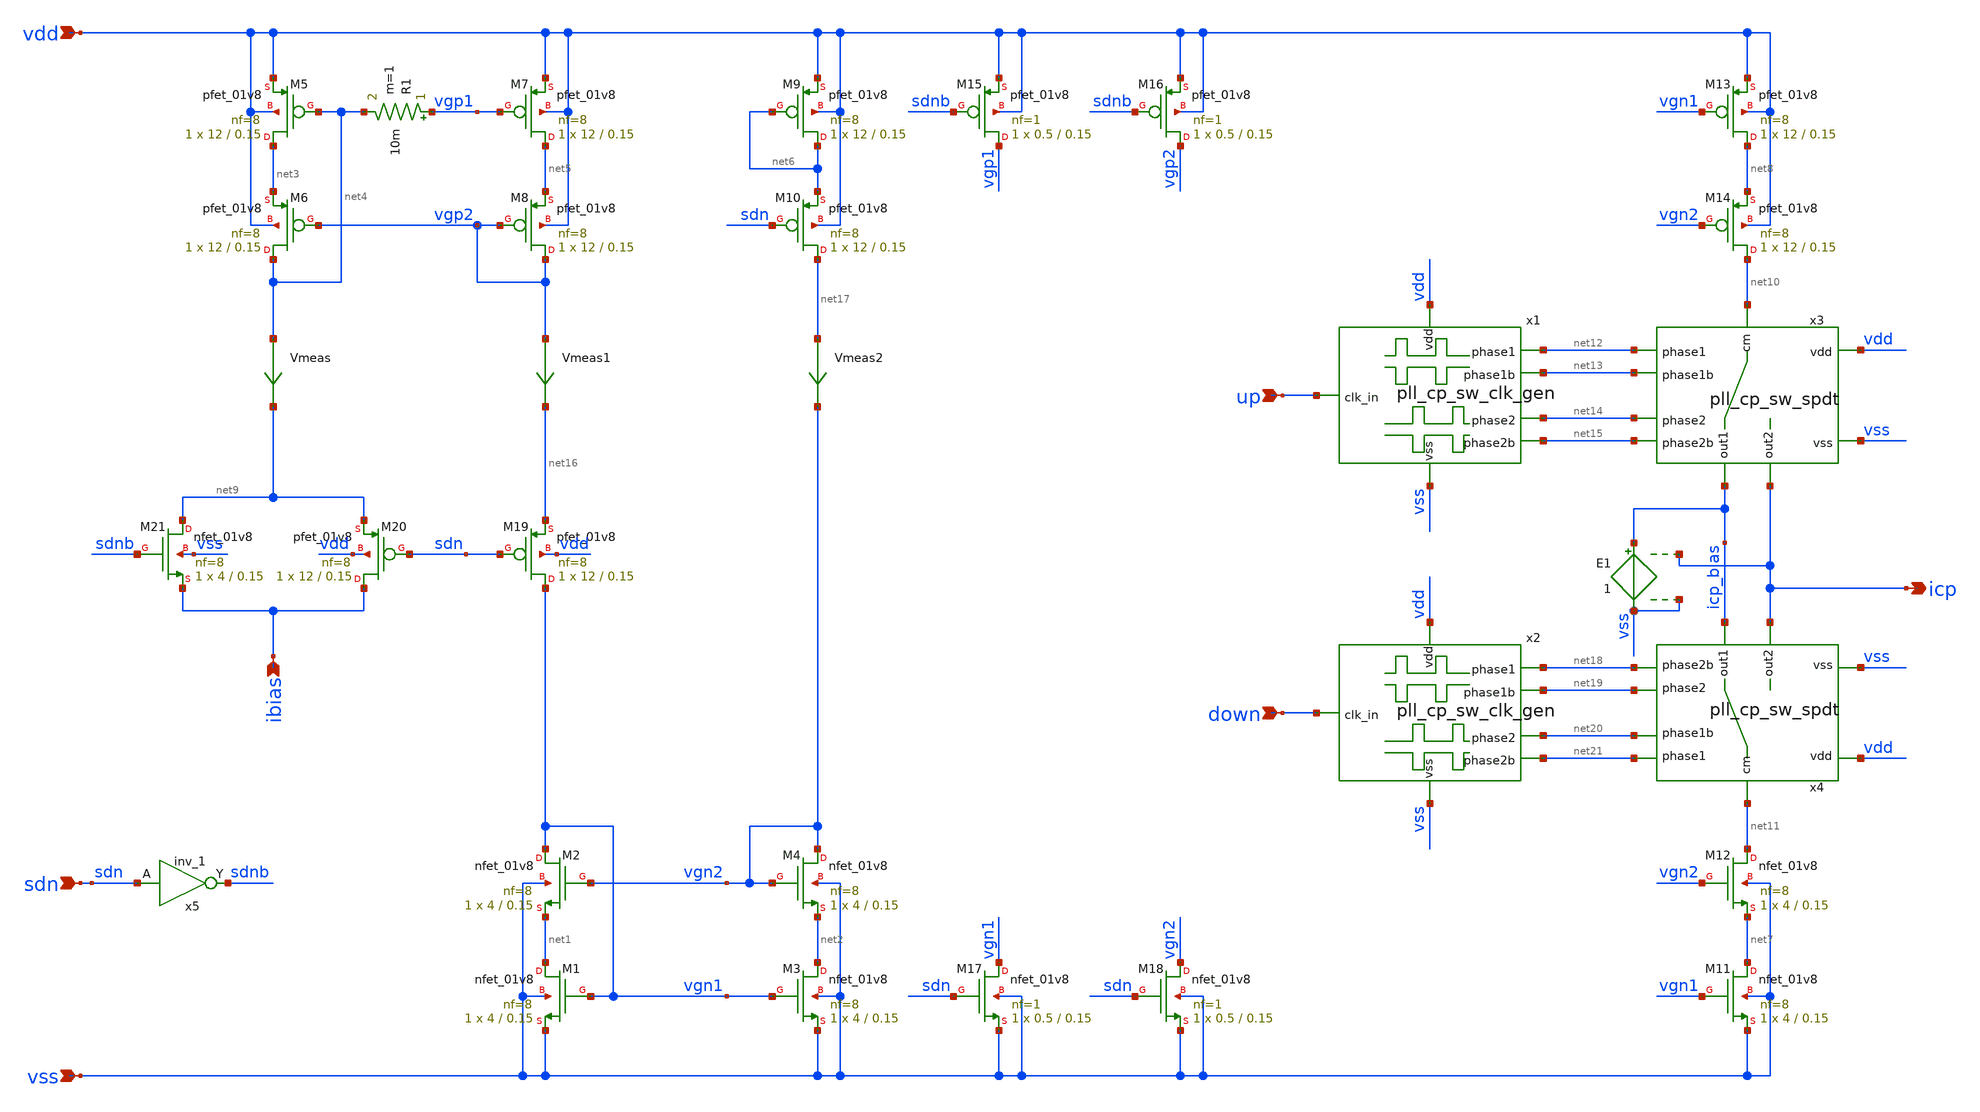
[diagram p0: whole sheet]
** sch_path: pll/pll_cp/xschem/pll_cp.sch
**.subckt pll_cp vdd vss up down ibias sdn icp
*.ipin vdd
*.ipin vss
*.ipin up
*.ipin down
*.ipin ibias
*.ipin sdn
*.opin icp
XM1 net1 vgn1 vss vss sky130_fd_pr__nfet_01v8 L=0.15 W=4 nf=8 ad='int((nf+1)/2) * W/nf * 0.29' as='int((nf+2)/2) * W/nf * 0.29'
+ pd='2*int((nf+1)/2) * (W/nf + 0.29)' ps='2*int((nf+2)/2) * (W/nf + 0.29)' nrd='0.29 / W' nrs='0.29 / W'
+ sa=0 sb=0 sd=0 mult=1 m=1
XM2 vgn1 vgn2 net1 vss sky130_fd_pr__nfet_01v8 L=0.15 W=4 nf=8 ad='int((nf+1)/2) * W/nf * 0.29' as='int((nf+2)/2) * W/nf * 0.29'
+ pd='2*int((nf+1)/2) * (W/nf + 0.29)' ps='2*int((nf+2)/2) * (W/nf + 0.29)' nrd='0.29 / W' nrs='0.29 / W'
+ sa=0 sb=0 sd=0 mult=1 m=1
XM3 net2 vgn1 vss vss sky130_fd_pr__nfet_01v8 L=0.15 W=4 nf=8 ad='int((nf+1)/2) * W/nf * 0.29' as='int((nf+2)/2) * W/nf * 0.29'
+ pd='2*int((nf+1)/2) * (W/nf + 0.29)' ps='2*int((nf+2)/2) * (W/nf + 0.29)' nrd='0.29 / W' nrs='0.29 / W'
+ sa=0 sb=0 sd=0 mult=1 m=1
XM4 vgn2 vgn2 net2 vss sky130_fd_pr__nfet_01v8 L=0.15 W=4 nf=8 ad='int((nf+1)/2) * W/nf * 0.29' as='int((nf+2)/2) * W/nf * 0.29'
+ pd='2*int((nf+1)/2) * (W/nf + 0.29)' ps='2*int((nf+2)/2) * (W/nf + 0.29)' nrd='0.29 / W' nrs='0.29 / W'
+ sa=0 sb=0 sd=0 mult=1 m=1
XM5 net3 net4 vdd vdd sky130_fd_pr__pfet_01v8 L=0.15 W=12 nf=8 ad='int((nf+1)/2) * W/nf * 0.29' as='int((nf+2)/2) * W/nf * 0.29'
+ pd='2*int((nf+1)/2) * (W/nf + 0.29)' ps='2*int((nf+2)/2) * (W/nf + 0.29)' nrd='0.29 / W' nrs='0.29 / W'
+ sa=0 sb=0 sd=0 mult=1 m=1
XM6 net4 vgp2 net3 vdd sky130_fd_pr__pfet_01v8 L=0.15 W=12 nf=8 ad='int((nf+1)/2) * W/nf * 0.29' as='int((nf+2)/2) * W/nf * 0.29'
+ pd='2*int((nf+1)/2) * (W/nf + 0.29)' ps='2*int((nf+2)/2) * (W/nf + 0.29)' nrd='0.29 / W' nrs='0.29 / W'
+ sa=0 sb=0 sd=0 mult=1 m=1
XM7 net5 vgp1 vdd vdd sky130_fd_pr__pfet_01v8 L=0.15 W=12 nf=8 ad='int((nf+1)/2) * W/nf * 0.29' as='int((nf+2)/2) * W/nf * 0.29'
+ pd='2*int((nf+1)/2) * (W/nf + 0.29)' ps='2*int((nf+2)/2) * (W/nf + 0.29)' nrd='0.29 / W' nrs='0.29 / W'
+ sa=0 sb=0 sd=0 mult=1 m=1
XM8 vgp2 vgp2 net5 vdd sky130_fd_pr__pfet_01v8 L=0.15 W=12 nf=8 ad='int((nf+1)/2) * W/nf * 0.29' as='int((nf+2)/2) * W/nf * 0.29'
+ pd='2*int((nf+1)/2) * (W/nf + 0.29)' ps='2*int((nf+2)/2) * (W/nf + 0.29)' nrd='0.29 / W' nrs='0.29 / W'
+ sa=0 sb=0 sd=0 mult=1 m=1
XM9 net6 net6 vdd vdd sky130_fd_pr__pfet_01v8 L=0.15 W=12 nf=8 ad='int((nf+1)/2) * W/nf * 0.29' as='int((nf+2)/2) * W/nf * 0.29'
+ pd='2*int((nf+1)/2) * (W/nf + 0.29)' ps='2*int((nf+2)/2) * (W/nf + 0.29)' nrd='0.29 / W' nrs='0.29 / W'
+ sa=0 sb=0 sd=0 mult=1 m=1
XM10 net17 sdn net6 vdd sky130_fd_pr__pfet_01v8 L=0.15 W=12 nf=8 ad='int((nf+1)/2) * W/nf * 0.29' as='int((nf+2)/2) * W/nf * 0.29'
+ pd='2*int((nf+1)/2) * (W/nf + 0.29)' ps='2*int((nf+2)/2) * (W/nf + 0.29)' nrd='0.29 / W' nrs='0.29 / W'
+ sa=0 sb=0 sd=0 mult=1 m=1
XM11 net7 vgn1 vss vss sky130_fd_pr__nfet_01v8 L=0.15 W=4 nf=8 ad='int((nf+1)/2) * W/nf * 0.29' as='int((nf+2)/2) * W/nf * 0.29'
+ pd='2*int((nf+1)/2) * (W/nf + 0.29)' ps='2*int((nf+2)/2) * (W/nf + 0.29)' nrd='0.29 / W' nrs='0.29 / W'
+ sa=0 sb=0 sd=0 mult=1 m=1
XM12 net11 vgn2 net7 vss sky130_fd_pr__nfet_01v8 L=0.15 W=4 nf=8 ad='int((nf+1)/2) * W/nf * 0.29' as='int((nf+2)/2) * W/nf * 0.29'
+ pd='2*int((nf+1)/2) * (W/nf + 0.29)' ps='2*int((nf+2)/2) * (W/nf + 0.29)' nrd='0.29 / W' nrs='0.29 / W'
+ sa=0 sb=0 sd=0 mult=1 m=1
XM13 net8 vgn1 vdd vdd sky130_fd_pr__pfet_01v8 L=0.15 W=12 nf=8 ad='int((nf+1)/2) * W/nf * 0.29' as='int((nf+2)/2) * W/nf * 0.29'
+ pd='2*int((nf+1)/2) * (W/nf + 0.29)' ps='2*int((nf+2)/2) * (W/nf + 0.29)' nrd='0.29 / W' nrs='0.29 / W'
+ sa=0 sb=0 sd=0 mult=1 m=1
XM14 net10 vgn2 net8 vdd sky130_fd_pr__pfet_01v8 L=0.15 W=12 nf=8 ad='int((nf+1)/2) * W/nf * 0.29' as='int((nf+2)/2) * W/nf * 0.29'
+ pd='2*int((nf+1)/2) * (W/nf + 0.29)' ps='2*int((nf+2)/2) * (W/nf + 0.29)' nrd='0.29 / W' nrs='0.29 / W'
+ sa=0 sb=0 sd=0 mult=1 m=1
XM15 vgp1 sdnb vdd vdd sky130_fd_pr__pfet_01v8 L=0.15 W=0.5 nf=1 ad='int((nf+1)/2) * W/nf * 0.29' as='int((nf+2)/2) * W/nf * 0.29'
+ pd='2*int((nf+1)/2) * (W/nf + 0.29)' ps='2*int((nf+2)/2) * (W/nf + 0.29)' nrd='0.29 / W' nrs='0.29 / W'
+ sa=0 sb=0 sd=0 mult=1 m=1
XM16 vgp2 sdnb vdd vdd sky130_fd_pr__pfet_01v8 L=0.15 W=0.5 nf=1 ad='int((nf+1)/2) * W/nf * 0.29' as='int((nf+2)/2) * W/nf * 0.29'
+ pd='2*int((nf+1)/2) * (W/nf + 0.29)' ps='2*int((nf+2)/2) * (W/nf + 0.29)' nrd='0.29 / W' nrs='0.29 / W'
+ sa=0 sb=0 sd=0 mult=1 m=1
XM17 vgn1 sdn vss vss sky130_fd_pr__nfet_01v8 L=0.15 W=0.5 nf=1 ad='int((nf+1)/2) * W/nf * 0.29' as='int((nf+2)/2) * W/nf * 0.29'
+ pd='2*int((nf+1)/2) * (W/nf + 0.29)' ps='2*int((nf+2)/2) * (W/nf + 0.29)' nrd='0.29 / W' nrs='0.29 / W'
+ sa=0 sb=0 sd=0 mult=1 m=1
XM18 vgn2 sdn vss vss sky130_fd_pr__nfet_01v8 L=0.15 W=0.5 nf=1 ad='int((nf+1)/2) * W/nf * 0.29' as='int((nf+2)/2) * W/nf * 0.29'
+ pd='2*int((nf+1)/2) * (W/nf + 0.29)' ps='2*int((nf+2)/2) * (W/nf + 0.29)' nrd='0.29 / W' nrs='0.29 / W'
+ sa=0 sb=0 sd=0 mult=1 m=1
x5 sdn vss vss vdd vdd sdnb sky130_fd_sc_hd__inv_1
XM19 vgn1 sdn net16 vdd sky130_fd_pr__pfet_01v8 L=0.15 W=12 nf=8 ad='int((nf+1)/2) * W/nf * 0.29' as='int((nf+2)/2) * W/nf * 0.29'
+ pd='2*int((nf+1)/2) * (W/nf + 0.29)' ps='2*int((nf+2)/2) * (W/nf + 0.29)' nrd='0.29 / W' nrs='0.29 / W'
+ sa=0 sb=0 sd=0 mult=1 m=1
XM20 ibias sdn net9 vdd sky130_fd_pr__pfet_01v8 L=0.15 W=12 nf=8 ad='int((nf+1)/2) * W/nf * 0.29' as='int((nf+2)/2) * W/nf * 0.29'
+ pd='2*int((nf+1)/2) * (W/nf + 0.29)' ps='2*int((nf+2)/2) * (W/nf + 0.29)' nrd='0.29 / W' nrs='0.29 / W'
+ sa=0 sb=0 sd=0 mult=1 m=1
XM21 net9 sdnb ibias vss sky130_fd_pr__nfet_01v8 L=0.15 W=4 nf=8 ad='int((nf+1)/2) * W/nf * 0.29' as='int((nf+2)/2) * W/nf * 0.29'
+ pd='2*int((nf+1)/2) * (W/nf + 0.29)' ps='2*int((nf+2)/2) * (W/nf + 0.29)' nrd='0.29 / W' nrs='0.29 / W'
+ sa=0 sb=0 sd=0 mult=1 m=1
R1 vgp1 net4 10m m=1
Vmeas net4 net9 0
.save i(vmeas)
Vmeas1 vgp2 net16 0
.save i(vmeas1)
Vmeas2 net17 vgn2 0
.save i(vmeas2)
E1 icp_bias vss icp vss 1
x1 vdd net12 net13 up net14 net15 vss pll_cp_sw_clk_gen
x2 vdd net18 net19 down net20 net21 vss pll_cp_sw_clk_gen
x3 net10 net12 net13 net14 net15 vdd icp_bias icp vss pll_cp_sw_spdt
x4 net11 net21 net20 net19 net18 vdd icp_bias icp vss pll_cp_sw_spdt
**** begin user architecture code

.options wnflag=1
.include $::SKYWATER_MODELS/cells/nfet_01v8/sky130_fd_pr__nfet_01v8__tt.corner.spice
.include $::SKYWATER_MODELS/cells/nfet_01v8_lvt/sky130_fd_pr__nfet_01v8_lvt__tt.corner.spice
.include $::SKYWATER_MODELS/cells/pfet_01v8/sky130_fd_pr__pfet_01v8__tt.corner.spice
.include $::SKYWATER_MODELS/cells/nfet_03v3_nvt/sky130_fd_pr__nfet_03v3_nvt__tt.corner.spice
.include $::SKYWATER_MODELS/cells/nfet_05v0_nvt/sky130_fd_pr__nfet_05v0_nvt__tt.corner.spice
.include $::SKYWATER_MODELS/cells/esd_nfet_01v8/sky130_fd_pr__esd_nfet_01v8__tt.corner.spice
.include $::SKYWATER_MODELS/cells/pfet_01v8_lvt/sky130_fd_pr__pfet_01v8_lvt__tt.corner.spice
.include $::SKYWATER_MODELS/cells/pfet_01v8_hvt/sky130_fd_pr__pfet_01v8_hvt__tt.corner.spice
.include $::SKYWATER_MODELS/cells/esd_pfet_g5v0d10v5/sky130_fd_pr__esd_pfet_g5v0d10v5__tt.corner.spice
.include $::SKYWATER_MODELS/cells/pfet_g5v0d10v5/sky130_fd_pr__pfet_g5v0d10v5__tt.corner.spice
.include $::SKYWATER_MODELS/cells/pfet_g5v0d16v0/sky130_fd_pr__pfet_g5v0d16v0__tt.corner.spice
.include $::SKYWATER_MODELS/cells/nfet_g5v0d10v5/sky130_fd_pr__nfet_g5v0d10v5__tt.corner.spice
.include $::SKYWATER_MODELS/cells/nfet_g5v0d16v0/sky130_fd_pr__nfet_g5v0d16v0__tt_discrete.corner.spice
.include $::SKYWATER_MODELS/cells/esd_nfet_g5v0d10v5/sky130_fd_pr__esd_nfet_g5v0d10v5__tt.corner.spice
.include $::SKYWATER_MODELS/models/corners/tt/nonfet.spice

.include $::SKYWATER_MODELS/cells/cap_var_hvt/sky130_fd_pr__cap_var_hvt.model.spice

* Mismatch parameters
.include $::SKYWATER_MODELS/cells/nfet_01v8/sky130_fd_pr__nfet_01v8__mismatch.corner.spice
.include $::SKYWATER_MODELS/cells/pfet_01v8/sky130_fd_pr__pfet_01v8__mismatch.corner.spice
.include $::SKYWATER_MODELS/cells/nfet_01v8_lvt/sky130_fd_pr__nfet_01v8_lvt__mismatch.corner.spice
.include $::SKYWATER_MODELS/cells/pfet_01v8_lvt/sky130_fd_pr__pfet_01v8_lvt__mismatch.corner.spice
.include $::SKYWATER_MODELS/cells/pfet_01v8_hvt/sky130_fd_pr__pfet_01v8_hvt__mismatch.corner.spice
.include $::SKYWATER_MODELS/cells/nfet_g5v0d10v5/sky130_fd_pr__nfet_g5v0d10v5__mismatch.corner.spice
.include $::SKYWATER_MODELS/cells/pfet_g5v0d10v5/sky130_fd_pr__pfet_g5v0d10v5__mismatch.corner.spice
.include $::SKYWATER_MODELS/cells/nfet_05v0_nvt/sky130_fd_pr__nfet_05v0_nvt__mismatch.corner.spice
.include $::SKYWATER_MODELS/cells/nfet_03v3_nvt/sky130_fd_pr__nfet_03v3_nvt__mismatch.corner.spice

* Resistor$::SKYWATER_MODELS/Capacitor
.include $::SKYWATER_MODELS/models/r+c/res_typical__cap_typical.spice
.include $::SKYWATER_MODELS/models/r+c/res_typical__cap_typical__lin.spice

* Special cells
.include $::SKYWATER_MODELS/models/corners/tt/specialized_cells.spice

* All models
.include $::SKYWATER_MODELS/models/all.spice

* Corner
.include $::SKYWATER_MODELS/models/corners/tt/rf.spice

* .include $::SKYWATER_STDCELLS/cells/
.include $::SKYWATER_STDCELLS/cells/and2/sky130_fd_sc_hd__and2_1.spice
.include $::SKYWATER_STDCELLS/cells/and2/sky130_fd_sc_hd__and2_2.spice
.include $::SKYWATER_STDCELLS_HS/cells/and2/sky130_fd_sc_hs__and2_1.spice
.include $::SKYWATER_STDCELLS_HS/cells/and2/sky130_fd_sc_hs__and2_2.spice

.include $::SKYWATER_STDCELLS/cells/or2/sky130_fd_sc_hd__or2_1.spice
.include $::SKYWATER_STDCELLS/cells/or2/sky130_fd_sc_hd__or2_2.spice
.include $::SKYWATER_STDCELLS_HS/cells/or2/sky130_fd_sc_hs__or2_1.spice
.include $::SKYWATER_STDCELLS_HS/cells/or2/sky130_fd_sc_hs__or2_2.spice

.include $::SKYWATER_STDCELLS/cells/buf/sky130_fd_sc_hd__buf_1.spice
.include $::SKYWATER_STDCELLS_HS/cells/buf/sky130_fd_sc_hs__buf_1.spice

.include $::SKYWATER_STDCELLS/cells/dfrbp/sky130_fd_sc_hd__dfrbp_1.spice
.include $::SKYWATER_STDCELLS/cells/dfrbp/sky130_fd_sc_hd__dfrbp_2.spice
.include $::SKYWATER_STDCELLS_HS/cells/dfrbp/sky130_fd_sc_hs__dfrbp_1.spice
.include $::SKYWATER_STDCELLS_HS/cells/dfrbp/sky130_fd_sc_hs__dfrbp_2.spice

.include $::SKYWATER_STDCELLS/cells/inv/sky130_fd_sc_hd__inv_1.spice
.include $::SKYWATER_STDCELLS/cells/inv/sky130_fd_sc_hd__inv_2.spice
.include $::SKYWATER_STDCELLS/cells/inv/sky130_fd_sc_hd__inv_4.spice
.include $::SKYWATER_STDCELLS/cells/inv/sky130_fd_sc_hd__inv_8.spice
.include $::SKYWATER_STDCELLS/cells/inv/sky130_fd_sc_hd__inv_16.spice
.include $::SKYWATER_STDCELLS_HS/cells/inv/sky130_fd_sc_hs__inv_1.spice
.include $::SKYWATER_STDCELLS_HS/cells/inv/sky130_fd_sc_hs__inv_2.spice
.include $::SKYWATER_STDCELLS_HS/cells/inv/sky130_fd_sc_hs__inv_4.spice
.include $::SKYWATER_STDCELLS_HS/cells/inv/sky130_fd_sc_hs__inv_8.spice
.include $::SKYWATER_STDCELLS_HS/cells/inv/sky130_fd_sc_hs__inv_16.spice

.include $::SKYWATER_STDCELLS/cells/mux2/sky130_fd_sc_hd__mux2_2.spice
.include $::SKYWATER_STDCELLS/cells/nand2/sky130_fd_sc_hd__nand2_1.spice

.include $::SKYWATER_STDCELLS/cells/tap/sky130_fd_sc_hd__tap_2.spice
.include $::SKYWATER_STDCELLS/cells/tapvpwrvgnd/sky130_fd_sc_hd__tapvpwrvgnd_1.spice

**** end user architecture code
**.ends

* expanding   symbol:  pll_cp_sw_clk_gen/xschem/pll_cp_sw_clk_gen.sym # of pins=7
** sym_path: pll/pll_cp_sw_clk_gen/xschem/pll_cp_sw_clk_gen.sym
** sch_path: pll/pll_cp_sw_clk_gen/xschem/pll_cp_sw_clk_gen.sch
.subckt pll_cp_sw_clk_gen vdd phase1 phase1b clk_in phase2 phase2b vss
*.ipin vdd
*.ipin vss
*.ipin clk_in
*.opin phase1
*.opin phase1b
*.opin phase2
*.opin phase2b
x1 net1 vdd vss clk_in net2 pll_nol_clkb
x2 phase2 vdd vss net2 phase2b pll_sync_clkb
x3 phase1 vdd vss net1 phase1b pll_sync_clkb
.ends


* expanding   symbol:  pll_cp_sw_spdt/xschem/pll_cp_sw_spdt.sym # of pins=9
** sym_path: pll/pll_cp_sw_spdt/xschem/pll_cp_sw_spdt.sym
** sch_path: pll/pll_cp_sw_spdt/xschem/pll_cp_sw_spdt.sch
.subckt pll_cp_sw_spdt cm phase1 phase1b phase2 phase2b vdd out1 out2 vss
*.ipin vdd
*.ipin vss
*.ipin phase1
*.ipin phase1b
*.ipin phase2
*.ipin phase2b
*.ipin cm
*.opin out2
*.opin out1
XM1 cm phase1 out1 vss sky130_fd_pr__nfet_01v8 L=0.15 W=2 nf=1 ad='int((nf+1)/2) * W/nf * 0.29' as='int((nf+2)/2) * W/nf * 0.29'
+ pd='2*int((nf+1)/2) * (W/nf + 0.29)' ps='2*int((nf+2)/2) * (W/nf + 0.29)' nrd='0.29 / W' nrs='0.29 / W'
+ sa=0 sb=0 sd=0 mult=1 m=1
XM2 cm phase1b out1 vdd sky130_fd_pr__pfet_01v8 L=0.15 W=4 nf=1 ad='int((nf+1)/2) * W/nf * 0.29' as='int((nf+2)/2) * W/nf * 0.29'
+ pd='2*int((nf+1)/2) * (W/nf + 0.29)' ps='2*int((nf+2)/2) * (W/nf + 0.29)' nrd='0.29 / W' nrs='0.29 / W'
+ sa=0 sb=0 sd=0 mult=1 m=1
XM3 cm phase2 out2 vss sky130_fd_pr__nfet_01v8 L=0.15 W=2 nf=1 ad='int((nf+1)/2) * W/nf * 0.29' as='int((nf+2)/2) * W/nf * 0.29'
+ pd='2*int((nf+1)/2) * (W/nf + 0.29)' ps='2*int((nf+2)/2) * (W/nf + 0.29)' nrd='0.29 / W' nrs='0.29 / W'
+ sa=0 sb=0 sd=0 mult=1 m=1
XM4 cm phase2b out2 vdd sky130_fd_pr__pfet_01v8 L=0.15 W=4 nf=1 ad='int((nf+1)/2) * W/nf * 0.29' as='int((nf+2)/2) * W/nf * 0.29'
+ pd='2*int((nf+1)/2) * (W/nf + 0.29)' ps='2*int((nf+2)/2) * (W/nf + 0.29)' nrd='0.29 / W' nrs='0.29 / W'
+ sa=0 sb=0 sd=0 mult=1 m=1
.ends


* expanding   symbol:  pll_nol_clkb/xschem/pll_nol_clkb.sym # of pins=5
** sym_path: pll/pll_nol_clkb/xschem/pll_nol_clkb.sym
** sch_path: pll/pll_nol_clkb/xschem/pll_nol_clkb.sch
.subckt pll_nol_clkb clk1 vdd vss clk clk2
*.opin clk1
*.opin clk2
*.ipin vdd
*.ipin vss
*.ipin clk
**** begin user architecture code
* .include $::SKYWATER_STDCELLS/cells/
.include $::SKYWATER_STDCELLS/cells/and2/sky130_fd_sc_hd__and2_1.spice
.include $::SKYWATER_STDCELLS/cells/and2/sky130_fd_sc_hd__and2_2.spice
.include $::SKYWATER_STDCELLS_HS/cells/and2/sky130_fd_sc_hs__and2_1.spice
.include $::SKYWATER_STDCELLS_HS/cells/and2/sky130_fd_sc_hs__and2_2.spice

.include $::SKYWATER_STDCELLS/cells/nand2/sky130_fd_sc_hd__nand2_1.spice
.include $::SKYWATER_STDCELLS/cells/nand2/sky130_fd_sc_hd__nand2_2.spice
.include $::SKYWATER_STDCELLS_HS/cells/nand2/sky130_fd_sc_hs__nand2_1.spice
.include $::SKYWATER_STDCELLS_HS/cells/nand2/sky130_fd_sc_hs__nand2_2.spice

.include $::SKYWATER_STDCELLS/cells/or2/sky130_fd_sc_hd__or2_1.spice
.include $::SKYWATER_STDCELLS/cells/or2/sky130_fd_sc_hd__or2_2.spice
.include $::SKYWATER_STDCELLS_HS/cells/or2/sky130_fd_sc_hs__or2_1.spice
.include $::SKYWATER_STDCELLS_HS/cells/or2/sky130_fd_sc_hs__or2_2.spice

.include $::SKYWATER_STDCELLS/cells/buf/sky130_fd_sc_hd__buf_1.spice
.include $::SKYWATER_STDCELLS_HS/cells/buf/sky130_fd_sc_hs__buf_1.spice

.include $::SKYWATER_STDCELLS/cells/dfrbp/sky130_fd_sc_hd__dfrbp_1.spice
.include $::SKYWATER_STDCELLS/cells/dfrbp/sky130_fd_sc_hd__dfrbp_2.spice
.include $::SKYWATER_STDCELLS_HS/cells/dfrbp/sky130_fd_sc_hs__dfrbp_1.spice
.include $::SKYWATER_STDCELLS_HS/cells/dfrbp/sky130_fd_sc_hs__dfrbp_2.spice

.include $::SKYWATER_STDCELLS/cells/inv/sky130_fd_sc_hd__inv_1.spice
.include $::SKYWATER_STDCELLS/cells/inv/sky130_fd_sc_hd__inv_2.spice
.include $::SKYWATER_STDCELLS/cells/inv/sky130_fd_sc_hd__inv_4.spice
.include $::SKYWATER_STDCELLS/cells/inv/sky130_fd_sc_hd__inv_8.spice
.include $::SKYWATER_STDCELLS/cells/inv/sky130_fd_sc_hd__inv_16.spice
.include $::SKYWATER_STDCELLS_HS/cells/inv/sky130_fd_sc_hs__inv_1.spice
.include $::SKYWATER_STDCELLS_HS/cells/inv/sky130_fd_sc_hs__inv_2.spice
.include $::SKYWATER_STDCELLS_HS/cells/inv/sky130_fd_sc_hs__inv_4.spice
.include $::SKYWATER_STDCELLS_HS/cells/inv/sky130_fd_sc_hs__inv_8.spice
.include $::SKYWATER_STDCELLS_HS/cells/inv/sky130_fd_sc_hs__inv_16.spice

.include $::SKYWATER_STDCELLS/cells/mux2/sky130_fd_sc_hd__mux2_2.spice
.include $::SKYWATER_STDCELLS/cells/nand2/sky130_fd_sc_hd__nand2_1.spice

.include $::SKYWATER_STDCELLS/cells/tap/sky130_fd_sc_hd__tap_2.spice
.include $::SKYWATER_STDCELLS/cells/tapvpwrvgnd/sky130_fd_sc_hd__tapvpwrvgnd_1.spice

**** end user architecture code
x3 clk1b vss vss vdd vdd clk1 sky130_fd_sc_hd__inv_1
x4 clk1 vss vss vdd vdd clk1fb sky130_fd_sc_hd__inv_1
x5 clk2b vss vss vdd vdd clk2 sky130_fd_sc_hd__inv_1
x6 clk2 vss vss vdd vdd clk2fb sky130_fd_sc_hd__inv_1
x7 clk vss vss vdd vdd clkb sky130_fd_sc_hd__inv_1
x1 clkb clk2fb vss vss vdd vdd clk1b sky130_fd_sc_hd__nand2_2
x2 clk1fb clk vss vss vdd vdd clk2b sky130_fd_sc_hd__nand2_2
* noconn vdd
* noconn vss
.ends


* expanding   symbol:  pll_sync_clkb/xschem/pll_sync_clkb.sym # of pins=5
** sym_path: pll/pll_sync_clkb/xschem/pll_sync_clkb.sym
** sch_path: pll/pll_sync_clkb/xschem/pll_sync_clkb.sch
.subckt pll_sync_clkb out_clk vdd vss in_clk out_clkb
*.opin out_clk
*.opin out_clkb
*.ipin vdd
*.ipin vss
*.ipin in_clk
**** begin user architecture code
* .include $::SKYWATER_STDCELLS/cells/
.include $::SKYWATER_STDCELLS/cells/and2/sky130_fd_sc_hd__and2_1.spice
.include $::SKYWATER_STDCELLS/cells/and2/sky130_fd_sc_hd__and2_2.spice
.include $::SKYWATER_STDCELLS_HS/cells/and2/sky130_fd_sc_hs__and2_1.spice
.include $::SKYWATER_STDCELLS_HS/cells/and2/sky130_fd_sc_hs__and2_2.spice

.include $::SKYWATER_STDCELLS/cells/nand2/sky130_fd_sc_hd__nand2_1.spice
.include $::SKYWATER_STDCELLS/cells/nand2/sky130_fd_sc_hd__nand2_2.spice
.include $::SKYWATER_STDCELLS_HS/cells/nand2/sky130_fd_sc_hs__nand2_1.spice
.include $::SKYWATER_STDCELLS_HS/cells/nand2/sky130_fd_sc_hs__nand2_2.spice

.include $::SKYWATER_STDCELLS/cells/or2/sky130_fd_sc_hd__or2_1.spice
.include $::SKYWATER_STDCELLS/cells/or2/sky130_fd_sc_hd__or2_2.spice
.include $::SKYWATER_STDCELLS_HS/cells/or2/sky130_fd_sc_hs__or2_1.spice
.include $::SKYWATER_STDCELLS_HS/cells/or2/sky130_fd_sc_hs__or2_2.spice

.include $::SKYWATER_STDCELLS/cells/buf/sky130_fd_sc_hd__buf_1.spice
.include $::SKYWATER_STDCELLS_HS/cells/buf/sky130_fd_sc_hs__buf_1.spice

.include $::SKYWATER_STDCELLS/cells/dfrbp/sky130_fd_sc_hd__dfrbp_1.spice
.include $::SKYWATER_STDCELLS/cells/dfrbp/sky130_fd_sc_hd__dfrbp_2.spice
.include $::SKYWATER_STDCELLS_HS/cells/dfrbp/sky130_fd_sc_hs__dfrbp_1.spice
.include $::SKYWATER_STDCELLS_HS/cells/dfrbp/sky130_fd_sc_hs__dfrbp_2.spice

.include $::SKYWATER_STDCELLS/cells/inv/sky130_fd_sc_hd__inv_1.spice
.include $::SKYWATER_STDCELLS/cells/inv/sky130_fd_sc_hd__inv_2.spice
.include $::SKYWATER_STDCELLS/cells/inv/sky130_fd_sc_hd__inv_4.spice
.include $::SKYWATER_STDCELLS/cells/inv/sky130_fd_sc_hd__inv_8.spice
.include $::SKYWATER_STDCELLS/cells/inv/sky130_fd_sc_hd__inv_16.spice
.include $::SKYWATER_STDCELLS_HS/cells/inv/sky130_fd_sc_hs__inv_1.spice
.include $::SKYWATER_STDCELLS_HS/cells/inv/sky130_fd_sc_hs__inv_2.spice
.include $::SKYWATER_STDCELLS_HS/cells/inv/sky130_fd_sc_hs__inv_4.spice
.include $::SKYWATER_STDCELLS_HS/cells/inv/sky130_fd_sc_hs__inv_8.spice
.include $::SKYWATER_STDCELLS_HS/cells/inv/sky130_fd_sc_hs__inv_16.spice

.include $::SKYWATER_STDCELLS/cells/mux2/sky130_fd_sc_hd__mux2_2.spice
.include $::SKYWATER_STDCELLS/cells/nand2/sky130_fd_sc_hd__nand2_1.spice

.include $::SKYWATER_STDCELLS/cells/tap/sky130_fd_sc_hd__tap_2.spice
.include $::SKYWATER_STDCELLS/cells/tapvpwrvgnd/sky130_fd_sc_hd__tapvpwrvgnd_1.spice

**** end user architecture code
x1 in_clk vss vss vdd vdd net1 sky130_fd_sc_hd__inv_2
x2 net1 vss vss vdd vdd net2 sky130_fd_sc_hd__inv_2
x4 stor_node vss vss vdd vdd out_clk sky130_fd_sc_hd__inv_1
x6 stor_node_b vss vss vdd vdd out_clkb sky130_fd_sc_hd__inv_1
x7 stor_node_b vss vss vdd vdd stor_node sky130_fd_sc_hd__inv_2
x9 stor_node vss vss vdd vdd stor_node_b sky130_fd_sc_hd__inv_2
x3 net2 vss vss vdd vdd stor_node sky130_fd_sc_hd__inv_1
x5 net1 vss vss vdd vdd stor_node_b sky130_fd_sc_hd__inv_1
* noconn vdd
* noconn vss
.ends

.end
